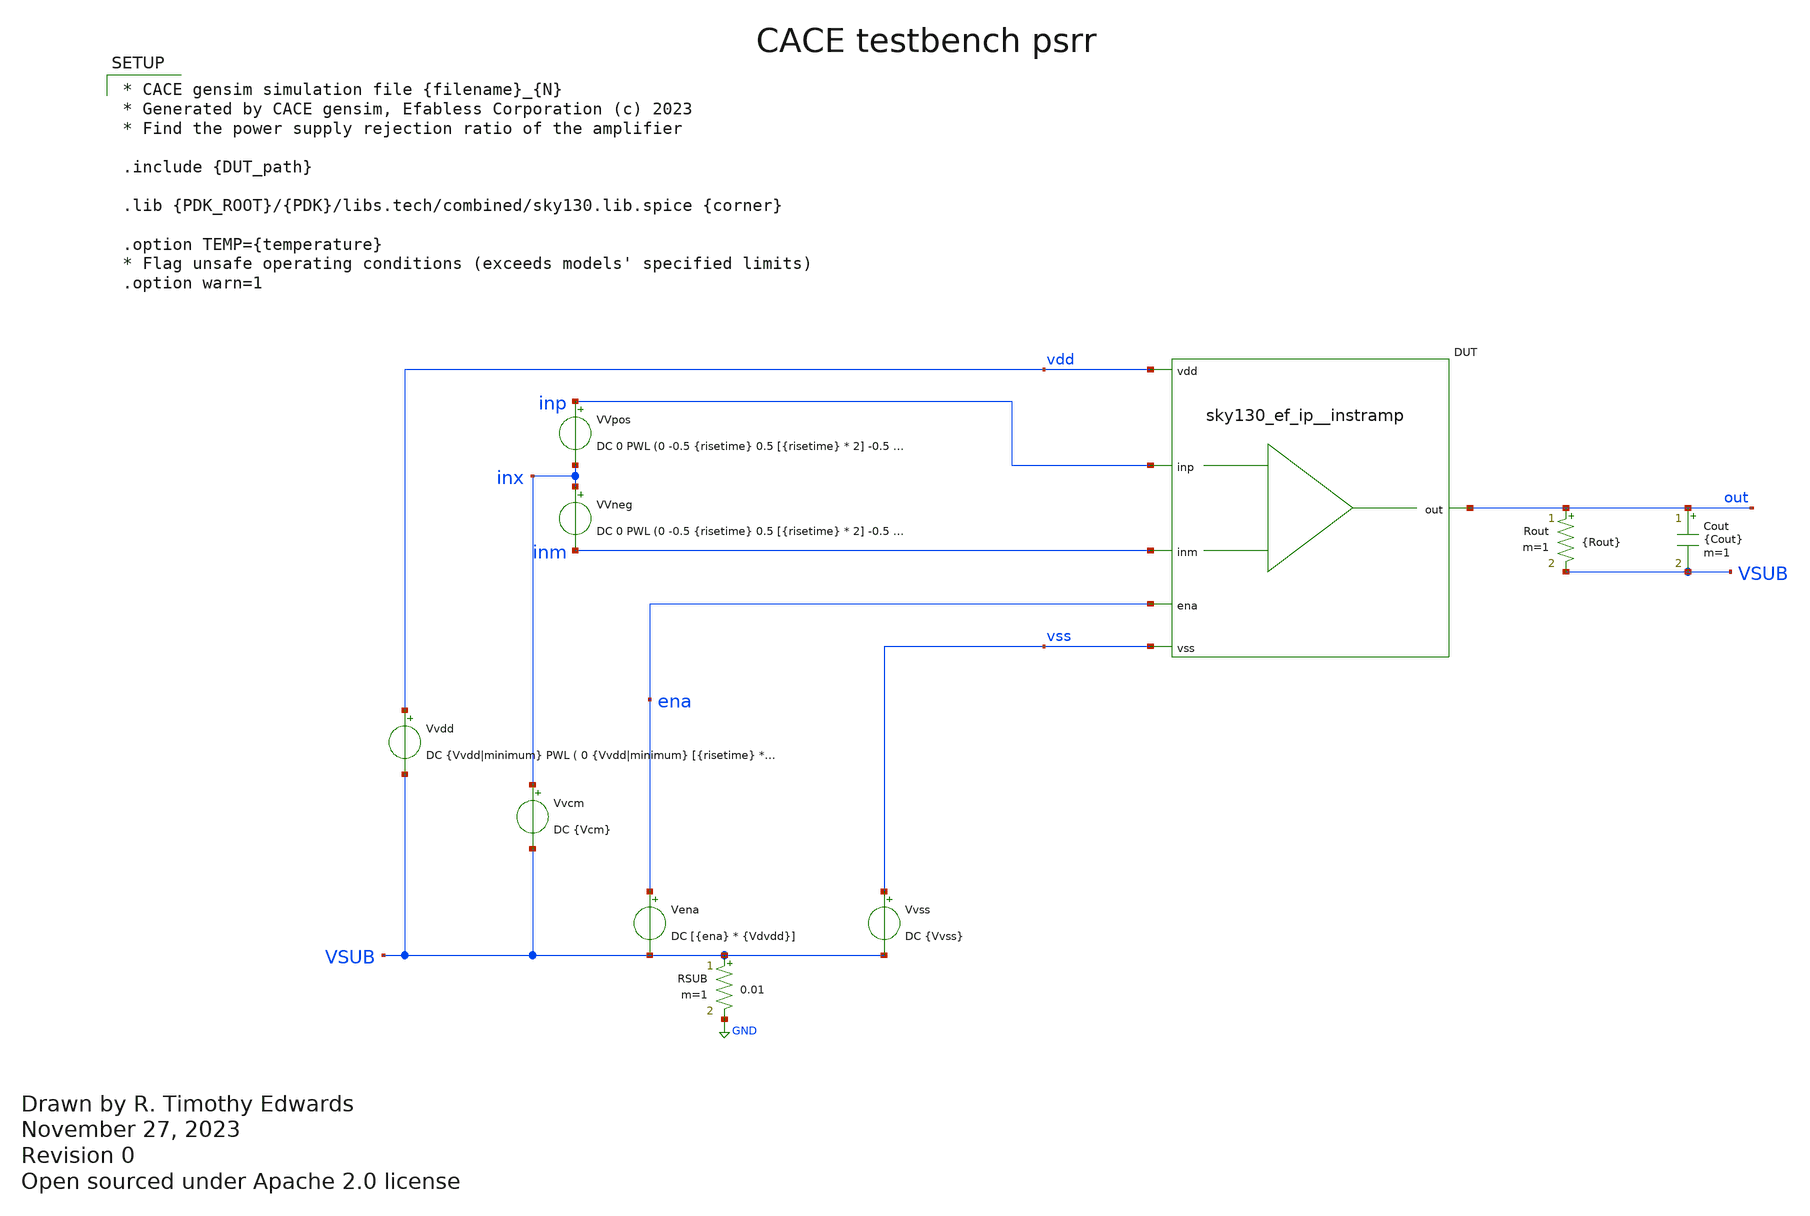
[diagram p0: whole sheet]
** sch_path: cace/psrr.sch
* Open sourced under Apache 2.0 license
**.subckt psrr
Vvdd vdd VSUB DC {Vvdd|minimum} PWL ( 0 {Vvdd|minimum} [{risetime} * 2] {Vvdd|minimum} [{risetime} *
+ 2 + 1e-9] {Vvdd|maximum} [{risetime} * 3] {Vvdd|maximum} )
Vena ena VSUB DC [{ena} * {Vdvdd}]
Vvss vss VSUB DC {Vvss}
Rout out VSUB {Rout} m=1
Cout out VSUB {Cout} m=1
Vvcm inx VSUB DC {Vcm}
RSUB VSUB GND 0.01 m=1
XDUT {PIN|vdd|vdd} {PIN|vss|vss} {PIN|inm|inm} {PIN|inp|inp} {PIN|out|out} {PIN|ena|ena} {DUT_name}
VVpos inp inx DC 0 PWL (0 -0.5 {risetime} 0.5 [{risetime} * 2] -0.5 [{risetime} * 3] 0.5 [{risetime}
+ * 4] -0.5 )
VVneg inx inm DC 0 PWL (0 -0.5 {risetime} 0.5 [{risetime} * 2] -0.5 [{risetime} * 3] 0.5 [{risetime}
+ * 4] -0.5 )
**** begin user architecture code

.control
** PSRR is defined as the change in input offset vs. change in power supply.
tran [{risetime} * 2 / 100] [{risetime} * 4]
meas tran vhigh1 FIND V(inp) WHEN V(out) = [{Vvdd|minimum} / 2] CROSS=1
meas tran vlow1 FIND V(inp) WHEN V(out) = [{Vvdd|minimum} / 2] CROSS=2
meas tran vhigh2 FIND V(inp) WHEN V(out) = [{Vvdd|maximum} / 2] CROSS=3
meas tran vlow2 FIND V(inp) WHEN V(out) = [{Vvdd|maximum} / 2] CROSS=4

let voffset1 = 0.5 * ($&vhigh1 + $&vlow1)
let voffset2 = 0.5 * ($&vhigh2 + $&vlow2)

let psrr = ($&voffset1 - $&voffset2) / ({Vvdd|maximum} - {Vvdd|minimum})
let psrrdb = 20 * log(abs($&psrr))

set wr_singlescale
wrdata {simpath}/{filename}_{N}.data $&psrrdb
quit
.endc



* CACE gensim simulation file {filename}_{N}
* Generated by CACE gensim, Efabless Corporation (c) 2023
* Find the power supply rejection ratio of the amplifier

.include {DUT_path}

.lib {PDK_ROOT}/{PDK}/libs.tech/combined/sky130.lib.spice {corner}

.option TEMP={temperature}
* Flag unsafe operating conditions (exceeds models' specified limits)
.option warn=1


**** end user architecture code
**.ends
.GLOBAL GND
.end
